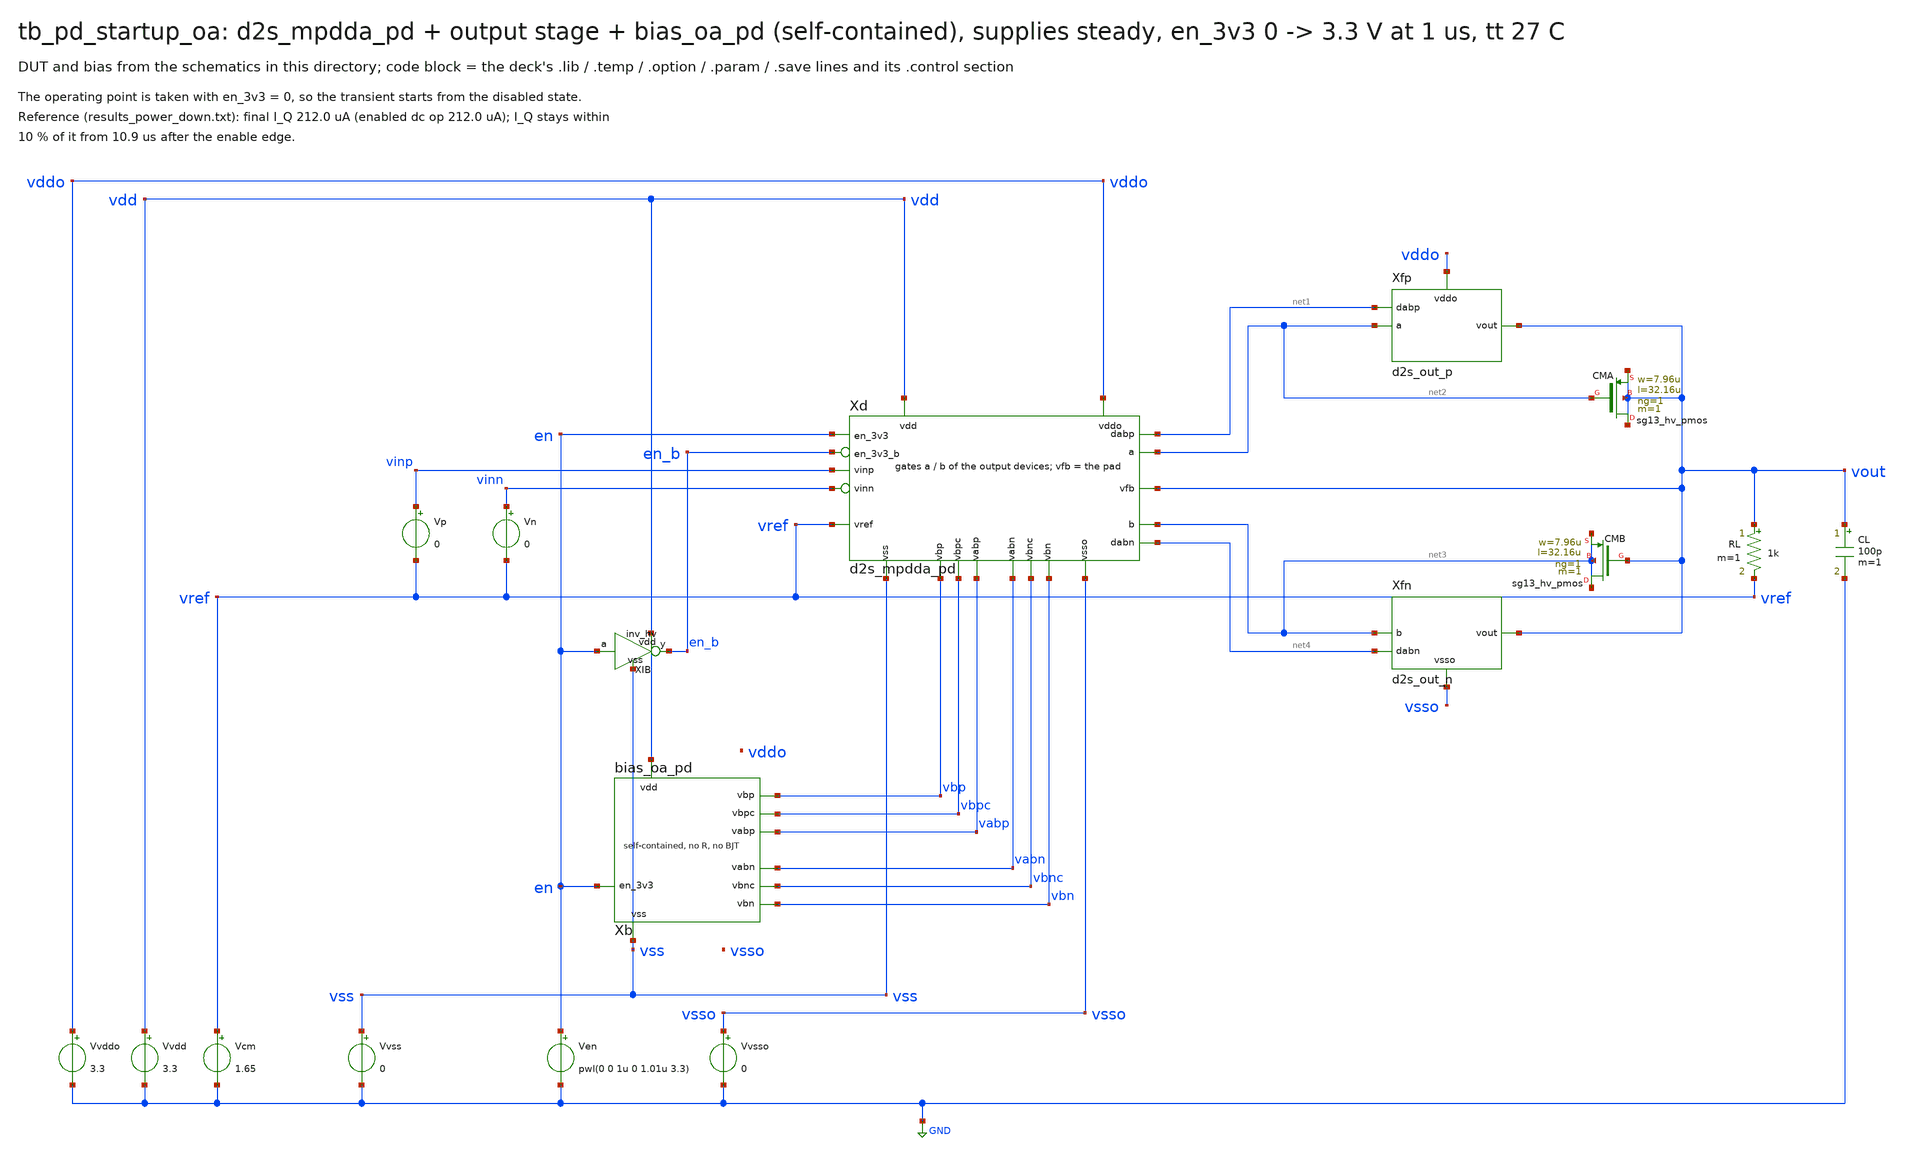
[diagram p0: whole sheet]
** sch_path: macros/sg13cmos5l_IOPadDiff2Single/testbenches/xschem/tb_pd_startup_oa.sch
**.subckt tb_pd_startup_oa
Vvdd vdd GND 3.3
Vvss vss GND 0
Vvddo vddo GND 3.3
Vvsso vsso GND 0
Ven en GND pwl(0 0 1u 0 1.01u 3.3)
Vcm vref GND 1.65
Xb vdd vss vbp vbn vbpc vbnc vabp vabn en bias_oa_pd
Xd vdd vss vddo vsso vinp vinn vref vout net2 net3 net1 net4 vbp vbn vbpc vbnc vabp vabn en en_b
+ d2s_mpdda_pd
Vp vinp vref 0
Vn vinn vref 0
RL vout vref 1k m=1
CL vout GND 100p m=1
XIB vdd vss en en_b inv_hv
Xfp vddo net2 vout net1 d2s_out_p
Xfn vsso net3 vout net4 d2s_out_n
XCMA vout net2 vout vout sg13_hv_pmos w=7.96u l=32.16u ng=1 m=1 mm_ok=1
XCMB net3 vout net3 net3 sg13_hv_pmos w=7.96u l=32.16u ng=1 m=1 mm_ok=1
**** begin user architecture code

.lib cornerMOShv.lib mos_tt
.lib cornerRES.lib res_typ
.lib cornerCAP.lib cap_typ
.temp 27
.option method=gear
.save v(vout) v(en) @n.xfp.xop.nsg13_hv_pmos[ids] v(xb.xc.vbr) v(xb.xc.ks)
.control
tran 20n 2m
let iq = abs(@n.xfp.xop.nsg13_hv_pmos[ids])
meas tran iqf find iq at=2m
let hi = 1.1*iqf
let lo = 0.9*iqf
meas tran t1 when iq=hi cross=last
meas tran t2 when iq=lo cross=last
print iqf t1 t2
if $?batchmode = 0
  plot iq
  plot v(vout) v(xb.xc.vbr) v(xb.xc.ks) xlimit 0 50u
end
.endc

**** end user architecture code
**.ends

* expanding   symbol:  bias_oa_pd.sym # of pins=9
** sym_path: macros/bias_oa_pd/schematic/xschem/bias_oa_pd.sym
** sch_path: macros/bias_oa_pd/schematic/xschem/bias_oa_pd.sch
.subckt bias_oa_pd vdd vss vbp vbn vbpc vbnc vabp vabn en_3v3
*.iopin vdd
*.iopin vss
*.opin vbp
*.opin vbn
*.opin vbpc
*.opin vbnc
*.opin vabp
*.opin vabn
*.ipin en_3v3
XMS1 ks en_3v3_b vdd vdd sg13_hv_pmos w=0.5u l=100u ng=1 m=1 mm_ok=1
XMS2 ks vbr vss vss sg13_hv_nmos w=10u l=1u ng=1 m=1 mm_ok=1
XMS3 vpc ks vss vss sg13_hv_nmos w=0.5u l=2u ng=1 m=1 mm_ok=1
XP0 vpg vpg vdd vdd sg13_hv_pmos w=2u l=8u ng=1 m=1 mm_ok=1
XP0C vpc vpc vpg vdd sg13_hv_pmos w=0.5u l=2u ng=1 m=1 mm_ok=1
XMC10 vpc vbr d10 vss sg13_hv_nmos w=10u l=1u ng=1 m=1 mm_ok=1
XM10 d10 vnc vres vss sg13_hv_nmos w=180u l=1u ng=8 m=1 mm_ok=1
XMCL vres vbr vss vss sg13_hv_nmos w=3.4u l=30u ng=1 m=1 mm_ok=1
XP8 c8 vpg vdd vdd sg13_hv_pmos w=16u l=8u ng=8 m=1 mm_ok=1
XP8C vnc vpc c8 vdd sg13_hv_pmos w=4u l=2u ng=2 m=1 mm_ok=1
XM11 vnc vnc vss vss sg13_hv_nmos w=90u l=1u ng=4 m=1 mm_ok=1
XP2 c2 vpg vdd vdd sg13_hv_pmos w=4u l=8u ng=2 m=1 mm_ok=1
XP2C vbr vpc c2 vdd sg13_hv_pmos w=1u l=2u ng=1 m=1 mm_ok=1
XMCS vbr vbr vss vss sg13_hv_nmos w=3.4u l=30u ng=1 m=1 mm_ok=1
XPO co vpg vdd vdd sg13_hv_pmos w=40u l=8u ng=20 m=1 mm_ok=1
XPOC iref vpc co vdd sg13_hv_pmos w=10u l=2u ng=5 m=1 mm_ok=1
XNI ni ni vss vss sg13_hv_nmos w=6u l=6u ng=1 m=1 mm_ok=1
XBPC vbpc vbpc vdd vdd sg13_hv_pmos w=1u l=4u ng=1 m=1 mm_ok=1
XNBPC vbpc ni vss vss sg13_hv_nmos w=2.4u l=6u ng=1 m=1 mm_ok=1
XBP vbp vbp vdd vdd sg13_hv_pmos w=5u l=6u ng=1 m=1 mm_ok=1
XNBP vbp ni vss vss sg13_hv_nmos w=6u l=6u ng=1 m=1 mm_ok=1
XNABP vabp ni vss vss sg13_hv_nmos w=6u l=6u ng=1 m=1 mm_ok=1
XPBNC vbnc vbp vdd vdd sg13_hv_pmos w=2u l=6u ng=1 m=1 mm_ok=1
XBNC vbnc vbnc vss vss sg13_hv_nmos w=1u l=8u ng=1 m=1 mm_ok=1
XPBN vbn vbp vdd vdd sg13_hv_pmos w=5u l=6u ng=1 m=1 mm_ok=1
XBN vbn vbn vss vss sg13_hv_nmos w=6u l=6u ng=1 m=1 mm_ok=1
XPABN vabn vbp vdd vdd sg13_hv_pmos w=5u l=6u ng=1 m=1 mm_ok=1
XSKS ks en_3v3_b vss vss sg13_hv_nmos w=1u l=0.45u ng=1 m=1 mm_ok=1
XSVPG vpg en_3v3 vdd vdd sg13_hv_pmos w=1u l=0.45u ng=1 m=1 mm_ok=1
XTDN ni en_3v3_b vss vss sg13_hv_nmos w=1u l=0.45u ng=1 m=1 mm_ok=1
XIP en_3v3_b en_3v3 vdd vdd sg13_hv_pmos w=1u l=0.45u ng=1 m=1 mm_ok=1
XIN en_3v3_b en_3v3 vss vss sg13_hv_nmos w=1u l=0.45u ng=1 m=1 mm_ok=1
XTGP ni en_3v3_b iref vdd sg13_hv_pmos w=1u l=0.45u ng=1 m=1 mm_ok=1
XTGN iref en_3v3 ni vss sg13_hv_nmos w=1u l=0.45u ng=1 m=1 mm_ok=1
.ends


* expanding   symbol:  d2s_mpdda_pd.sym # of pins=20
** sym_path: macros/sg13cmos5l_IOPadDiff2Single/schematic/xschem/d2s_mpdda_pd.sym
** sch_path: macros/sg13cmos5l_IOPadDiff2Single/schematic/xschem/d2s_mpdda_pd.sch
.subckt d2s_mpdda_pd vdd vss vddo vsso vinp vinn vref vfb a b dabp dabn vbp vbn vbpc vbnc vabp vabn
+ en_3v3 en_3v3_b
*.iopin vdd
*.iopin vss
*.iopin vddo
*.iopin vsso
*.ipin vinp
*.ipin vinn
*.ipin vref
*.ipin vfb
*.ipin vbp
*.ipin vbn
*.ipin vbpc
*.ipin vbnc
*.ipin vabp
*.ipin vabn
*.ipin en_3v3
*.ipin en_3v3_b
*.opin a
*.opin b
*.iopin dabp
*.iopin dabn
XA x y vinp vref vdd vss vbp unit_r2
XB x y vref vinn vdd vss vbp unit_r2
XC1 x y vref vfb vdd vss vbp unit_r2
XC2 x y vref vfb vdd vss vbp unit_r2
XFNL l2 vabn l1 vss sg13_hv_nmos w=4.4u l=1u ng=1 m=1 mm_ok=1
XCX l1 vbnc x vss sg13_hv_nmos w=30u l=3u ng=2 m=1 mm_ok=1
XSX x vbn vss vss sg13_hv_nmos w=36u l=6u ng=6 m=1 mm_ok=1
XPL pl l2 vdd vdd sg13_hv_pmos w=24u l=4u ng=4 m=1 mm_ok=1
XPCL l2 vbpc pl vdd sg13_hv_pmos w=30u l=3u ng=2 m=1 mm_ok=1
XFPL l1 vabp l2 vdd sg13_hv_pmos w=6.66u l=0.6u ng=1 m=1 mm_ok=1
XPR pr l2 vdd vdd sg13_hv_pmos w=24u l=4u ng=4 m=1 mm_ok=1
XPCR a vbpc pr vdd sg13_hv_pmos w=30u l=3u ng=2 m=1 mm_ok=1
XABP b vabp a vdd sg13_hv_pmos w=6.66u l=0.6u ng=1 m=1 mm_ok=1
XABN a vabn b vss sg13_hv_nmos w=4.4u l=1u ng=1 m=1 mm_ok=1
XCY b vbnc y vss sg13_hv_nmos w=30u l=3u ng=2 m=1 mm_ok=1
XSY y vbn vss vss sg13_hv_nmos w=36u l=6u ng=6 m=1 mm_ok=1
XSABP vabp en_3v3 vdd vdd sg13_hv_pmos w=1u l=0.45u ng=1 m=1 mm_ok=1
XSA a en_3v3 vddo vdd sg13_hv_pmos w=1u l=0.45u ng=1 m=1 mm_ok=1
XSABN vabn en_3v3_b vss vss sg13_hv_nmos w=1u l=0.45u ng=1 m=1 mm_ok=1
XSB b en_3v3_b vsso vss sg13_hv_nmos w=1u l=0.45u ng=1 m=1 mm_ok=1
XRP2 vabp vabp dabp vdd sg13_hv_pmos w=6.66u l=0.6u ng=1 m=1 mm_ok=1
XRN2 vabn vabn dabn vss sg13_hv_nmos w=4.4u l=1u ng=1 m=1 mm_ok=1
XMDT[3] vdd vdd vdd vdd sg13_hv_pmos w=20u l=1u ng=2 m=1 mm_ok=1
XMDT[2] vdd vdd vdd vdd sg13_hv_pmos w=20u l=1u ng=2 m=1 mm_ok=1
XMDT[1] vdd vdd vdd vdd sg13_hv_pmos w=20u l=1u ng=2 m=1 mm_ok=1
XMDT[0] vdd vdd vdd vdd sg13_hv_pmos w=20u l=1u ng=2 m=1 mm_ok=1
XMDTL[2] vdd vbp vdd vdd sg13_hv_pmos w=5u l=6u ng=1 m=1 mm_ok=1
XMDTL[1] vdd vbp vdd vdd sg13_hv_pmos w=5u l=6u ng=1 m=1 mm_ok=1
XMDTL[0] vdd vbp vdd vdd sg13_hv_pmos w=5u l=6u ng=1 m=1 mm_ok=1
XMDL[3] vdd l2 vdd vdd sg13_hv_pmos w=1u l=4u ng=1 m=1 mm_ok=1
XMDL[2] vdd l2 vdd vdd sg13_hv_pmos w=1u l=4u ng=1 m=1 mm_ok=1
XMDL[1] vdd l2 vdd vdd sg13_hv_pmos w=1u l=4u ng=1 m=1 mm_ok=1
XMDL[0] vdd l2 vdd vdd sg13_hv_pmos w=1u l=4u ng=1 m=1 mm_ok=1
XMDPC vdd vbpc vdd vdd sg13_hv_pmos w=1u l=4u ng=1 m=1 mm_ok=1
XMDABP[1] vdd vdd vdd vdd sg13_hv_pmos w=6.66u l=0.6u ng=1 m=1 mm_ok=1
XMDABP[0] vdd vdd vdd vdd sg13_hv_pmos w=6.66u l=0.6u ng=1 m=1 mm_ok=1
XMDABN[1] vss vss vss vss sg13_hv_nmos w=4.4u l=1u ng=1 m=1 mm_ok=1
XMDABN[0] vss vss vss vss sg13_hv_nmos w=4.4u l=1u ng=1 m=1 mm_ok=1
XMDCN[3] vbnc vbnc vbnc vss sg13_hv_nmos w=2u l=3u ng=1 m=1 mm_ok=1
XMDCN[2] vbnc vbnc vbnc vss sg13_hv_nmos w=2u l=3u ng=1 m=1 mm_ok=1
XMDCN[1] vbnc vbnc vbnc vss sg13_hv_nmos w=2u l=3u ng=1 m=1 mm_ok=1
XMDCN[0] vbnc vbnc vbnc vss sg13_hv_nmos w=2u l=3u ng=1 m=1 mm_ok=1
XMDSK[3] vbn vbn vbn vss sg13_hv_nmos w=2u l=6u ng=1 m=1 mm_ok=1
XMDSK[2] vbn vbn vbn vss sg13_hv_nmos w=2u l=6u ng=1 m=1 mm_ok=1
XMDSK[1] vbn vbn vbn vss sg13_hv_nmos w=2u l=6u ng=1 m=1 mm_ok=1
XMDSK[0] vbn vbn vbn vss sg13_hv_nmos w=2u l=6u ng=1 m=1 mm_ok=1
XMDBNT vbn vbn vbn vss sg13_hv_nmos w=6u l=6u ng=1 m=1 mm_ok=1
XRD[1] vss vss vss rhigh w=0.5u l=12.65u m=1 b=0 mm_ok=1
XRD[0] vss vss vss rhigh w=0.5u l=12.65u m=1 b=0 mm_ok=1
.ends


* expanding   symbol:  inv_hv.sym # of pins=4
** sym_path: macros/hv_logic/schematic/xschem/inv_hv.sym
** sch_path: macros/hv_logic/schematic/xschem/inv_hv.sch
.subckt inv_hv vdd vss a y
*.iopin vdd
*.iopin vss
*.ipin a
*.opin y
XP y a vdd vdd sg13_hv_pmos w=1u l=0.45u ng=1 m=1 mm_ok=1
XN y a vss vss sg13_hv_nmos w=1u l=0.45u ng=1 m=1 mm_ok=1
.ends


* expanding   symbol:  d2s_out_p.sym # of pins=4
** sym_path: macros/sg13cmos5l_IOPadDiff2Single/schematic/xschem/d2s_out_p.sym
** sch_path: macros/sg13cmos5l_IOPadDiff2Single/schematic/xschem/d2s_out_p.sch
.subckt d2s_out_p vddo a vout dabp
*.iopin vddo
*.ipin a
*.iopin vout
*.iopin dabp
XOP vout a vddo vddo sg13_hv_pmos w=546.12u l=0.6u ng=82 m=1 mm_ok=1
XRP1 dabp dabp vddo vddo sg13_hv_pmos w=13.32u l=0.6u ng=2 m=1 mm_ok=1
XRPD dabp vddo vddo vddo sg13_hv_pmos w=13.32u l=0.6u ng=2 m=1 mm_ok=1
.ends


* expanding   symbol:  d2s_out_n.sym # of pins=4
** sym_path: macros/sg13cmos5l_IOPadDiff2Single/schematic/xschem/d2s_out_n.sym
** sch_path: macros/sg13cmos5l_IOPadDiff2Single/schematic/xschem/d2s_out_n.sch
.subckt d2s_out_n vsso b vout dabn
*.iopin vsso
*.ipin b
*.iopin vout
*.iopin dabn
XON vout b vsso vsso sg13_hv_nmos w=299.2u l=1u ng=68 m=1 mm_ok=1
XRN1 dabn dabn vsso vsso sg13_hv_nmos w=8.8u l=1u ng=2 m=1 mm_ok=1
.ends


* expanding   symbol:  unit_r2.sym # of pins=7
** sym_path: sudelbuecher/design_considerations/class_ab_pad_driver/improvements/xschem/unit_r2.sym
** sch_path: sudelbuecher/design_considerations/class_ab_pad_driver/improvements/xschem/unit_r2.sch
.subckt unit_r2 x y gp gn vdd vss vbp
*.opin x
*.opin y
*.ipin gp
*.ipin gn
*.iopin vdd
*.iopin vss
*.ipin vbp
XTa sa vbp vdd vdd sg13_hv_pmos w=5u l=6u ng=1 m=1 mm_ok=1
XTb sb vbp vdd vdd sg13_hv_pmos w=5u l=6u ng=1 m=1 mm_ok=1
XMa y gp sa sa sg13_hv_pmos w=20u l=1u ng=2 m=1 mm_ok=1
XMb x gn sb sb sg13_hv_pmos w=20u l=1u ng=2 m=1 mm_ok=1
XR sa sb vss rhigh w=0.5u l=50.6u m=1 b=0 mm_ok=1
.ends

.GLOBAL GND
.end
